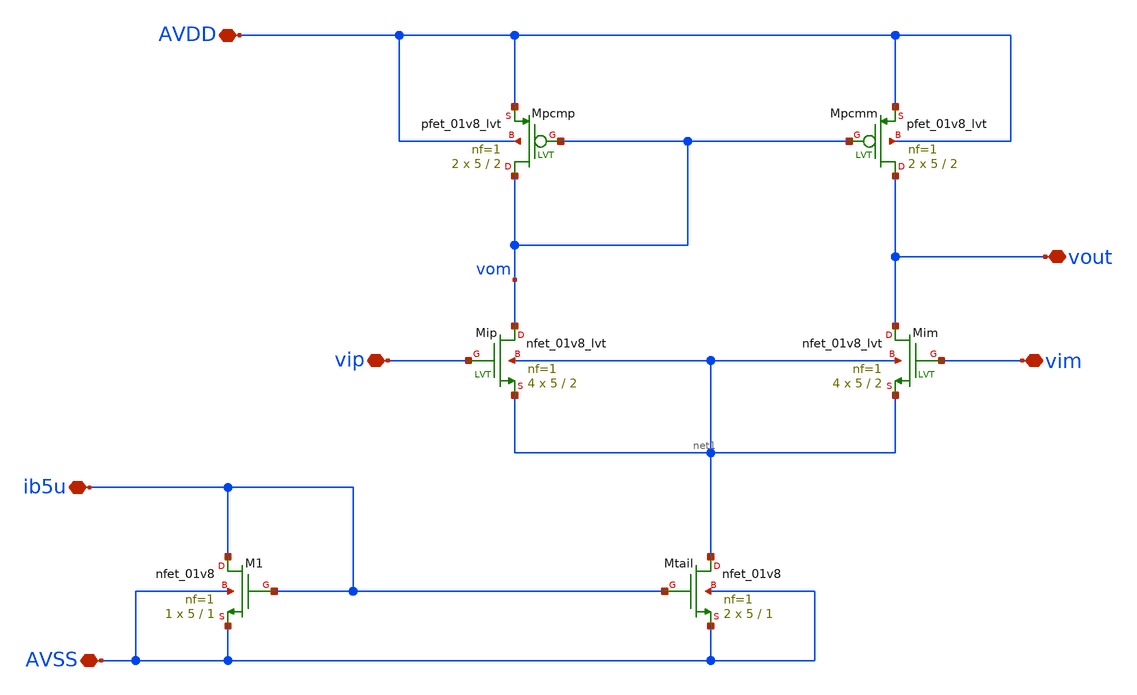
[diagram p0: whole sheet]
** sch_path: xschem/opamp_nmos.sch
**.subckt opamp_nmos vip vim vout AVDD ib5u AVSS
*.iopin vip
*.iopin vim
*.iopin vout
*.iopin AVDD
*.iopin ib5u
*.iopin AVSS
XMip vom vip net1 net1 sky130_fd_pr__nfet_01v8_lvt L=2 W=5 nf=1 ad='int((1 + 1)/2) * 5 / 1 * 0.29' as='int((1 + 2)/2) * 5 / 1 * 0.29'
+ pd='2*int((1 + 1)/2) * (5 / 1 + 0.29)' ps='2*int((1 + 2)/2) * (5 / 1 + 0.29)' nrd='0.29 / 5 ' nrs='0.29 / 5 '
+ sa=0 sb=0 sd=0 mult=4 m=4
XMim vout vim net1 net1 sky130_fd_pr__nfet_01v8_lvt L=2 W=5 nf=1 ad='int((1 + 1)/2) * 5 / 1 * 0.29' as='int((1 + 2)/2) * 5 / 1 * 0.29'
+ pd='2*int((1 + 1)/2) * (5 / 1 + 0.29)' ps='2*int((1 + 2)/2) * (5 / 1 + 0.29)' nrd='0.29 / 5 ' nrs='0.29 / 5 '
+ sa=0 sb=0 sd=0 mult=4 m=4
XM1 ib5u ib5u AVSS AVSS sky130_fd_pr__nfet_01v8 L=1 W=5 nf=1 ad='int((1 + 1)/2) * 5 / 1 * 0.29' as='int((1 + 2)/2) * 5 / 1 * 0.29'
+ pd='2*int((1 + 1)/2) * (5 / 1 + 0.29)' ps='2*int((1 + 2)/2) * (5 / 1 + 0.29)' nrd='0.29 / 5 ' nrs='0.29 / 5 '
+ sa=0 sb=0 sd=0 mult=1 m=1
XMtail net1 ib5u AVSS AVSS sky130_fd_pr__nfet_01v8 L=1 W=5 nf=1 ad='int((1 + 1)/2) * 5 / 1 * 0.29' as='int((1 + 2)/2) * 5 / 1 * 0.29'
+ pd='2*int((1 + 1)/2) * (5 / 1 + 0.29)' ps='2*int((1 + 2)/2) * (5 / 1 + 0.29)' nrd='0.29 / 5 ' nrs='0.29 / 5 '
+ sa=0 sb=0 sd=0 mult=2 m=2
XMpcmp vom vom AVDD AVDD sky130_fd_pr__pfet_01v8_lvt L=2 W=5 nf=1 ad='int((1 + 1)/2) * 5 / 1 * 0.29'
+ as='int((1 + 2)/2) * 5 / 1 * 0.29' pd='2*int((1 + 1)/2) * (5 / 1 + 0.29)' ps='2*int((1 + 2)/2) * (5 / 1 + 0.29)'
+ nrd='0.29 / 5 ' nrs='0.29 / 5 ' sa=0 sb=0 sd=0 mult=2 m=2
XMpcmm vout vom AVDD AVDD sky130_fd_pr__pfet_01v8_lvt L=2 W=5 nf=1 ad='int((1 + 1)/2) * 5 / 1 * 0.29'
+ as='int((1 + 2)/2) * 5 / 1 * 0.29' pd='2*int((1 + 1)/2) * (5 / 1 + 0.29)' ps='2*int((1 + 2)/2) * (5 / 1 + 0.29)'
+ nrd='0.29 / 5 ' nrs='0.29 / 5 ' sa=0 sb=0 sd=0 mult=2 m=2
**.ends
.end
